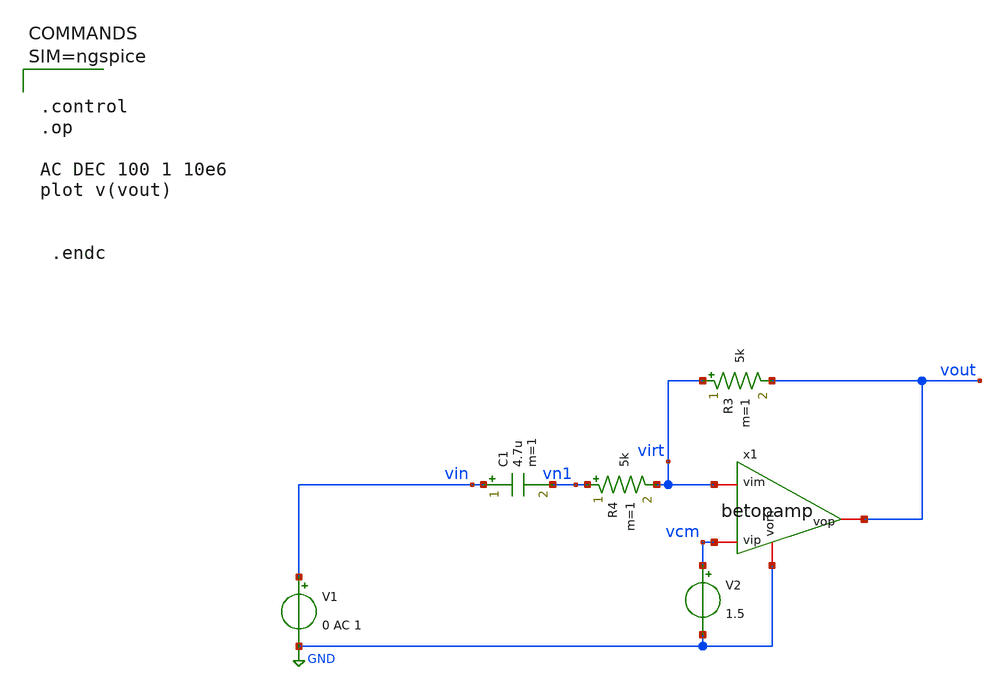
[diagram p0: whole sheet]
** sch_path: xschem/mictest_opamp.sch
**.subckt mictest_opamp
V1 vin GND 0 AC 1
C1 vin vn1 4.7u m=1
R3 virt vout 5k m=1
V2 vcm GND 1.5
R4 vn1 virt 5k m=1
x1 vout vcm virt GND betopamp
**** begin user architecture code



.control
.op

AC DEC 100 1 10e6
plot v(vout)


 .endc



**** end user architecture code
**.ends

* expanding   symbol:  betopamp.sym # of pins=4
** sym_path: xschem/betopamp.sym
** sch_path: xschem/betopamp.sch
.subckt betopamp vop vip vim vom
*.iopin vip
*.iopin vim
*.iopin vop
*.iopin vom
E1 vop vom vip vim 1000
.ends

.GLOBAL GND
.end
